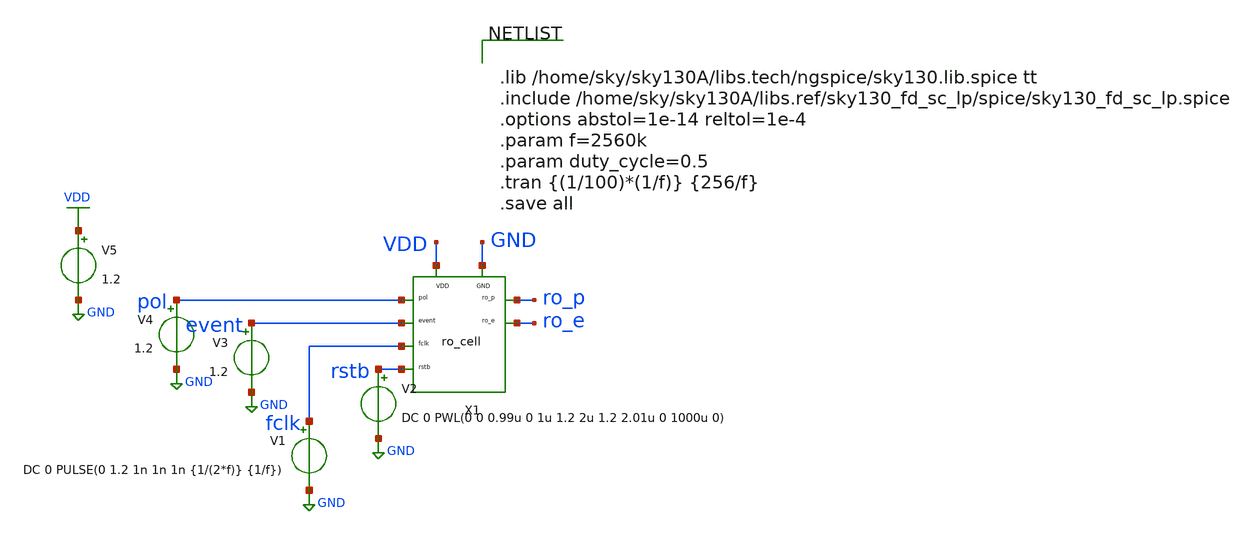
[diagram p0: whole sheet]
** sch_path: xschem/readout/ro_cell_tb.sch
**.subckt ro_cell_tb
X1 pol event fclk rstb ro_p ro_e VDD GND ro_cell
V1 fclk GND DC 0 PULSE(0 1.2 1n 1n 1n {1/(2*f)} {1/f})
V2 rstb GND DC 0 PWL(0 0 0.99u 0 1u 1.2 2u 1.2 2.01u 0 1000u 0)
V3 event GND 1.2
V4 pol GND 1.2
V5 VDD GND 1.2
**** begin user architecture code


.lib /home/sky/sky130A/libs.tech/ngspice/sky130.lib.spice tt
.include /home/sky/sky130A/libs.ref/sky130_fd_sc_lp/spice/sky130_fd_sc_lp.spice
.options abstol=1e-14 reltol=1e-4
.param f=2560k
.param duty_cycle=0.5
.tran {(1/100)*(1/f)} {256/f}
.save all


**** end user architecture code
**.ends

* expanding   symbol:  readout/ro_cell.sym # of pins=8
** sym_path: xschem/readout/ro_cell.sym
** sch_path: xschem/readout/ro_cell.sch
.subckt ro_cell pol event fclk rstb ro_p ro_e VDD GND
*.ipin pol
*.ipin event
*.ipin fclk
*.ipin rstb
*.iopin VDD
*.iopin GND
*.opin ro_p
*.opin ro_e
x1 fclk pol rstb GND GND VDD VDD ro_p sky130_fd_sc_lp__dfrtn_1
x2 fclk event rstb GND GND VDD VDD ro_e sky130_fd_sc_lp__dfrtn_1
.ends

.GLOBAL GND
.GLOBAL VDD
.end
